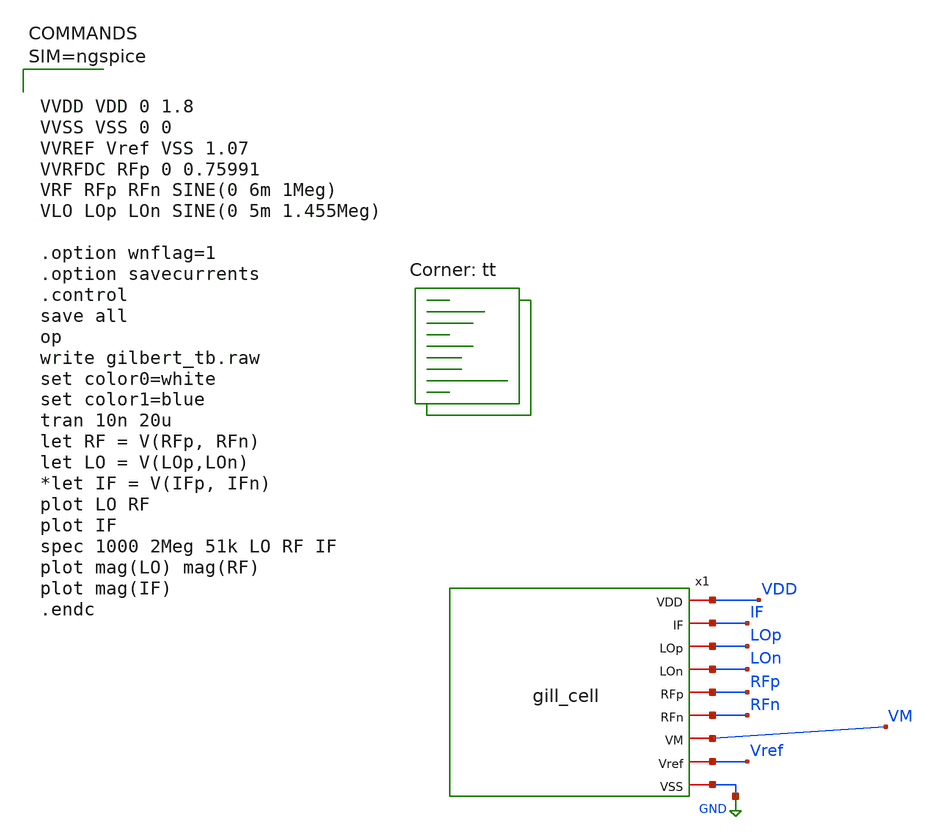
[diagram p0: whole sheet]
** sch_path: hw07/xschem/gilbert_tb.sch
**.subckt gilbert_tb
x1 VDD IF LOp LOn RFp RFn VM Vref GND gill_cell
**** begin user architecture code



VVDD VDD 0 1.8
VVSS VSS 0 0
VVREF Vref VSS 1.07
VVRFDC RFp 0 0.75991
VRF RFp RFn SINE(0 6m 1Meg)
VLO LOp LOn SINE(0 5m 1.455Meg)

.option wnflag=1
.option savecurrents
.control
save all
op
write gilbert_tb.raw
set color0=white
set color1=blue
tran 10n 20u
let RF = V(RFp, RFn)
let LO = V(LOp,LOn)
*let IF = V(IFp, IFn)
plot LO RF
plot IF
spec 1000 2Meg 51k LO RF IF
plot mag(LO) mag(RF)
plot mag(IF)
.endc



.lib $::SKYWATER_MODELS/sky130.lib.spice tt
**** end user architecture code
**.ends
.GLOBAL GND
.end
